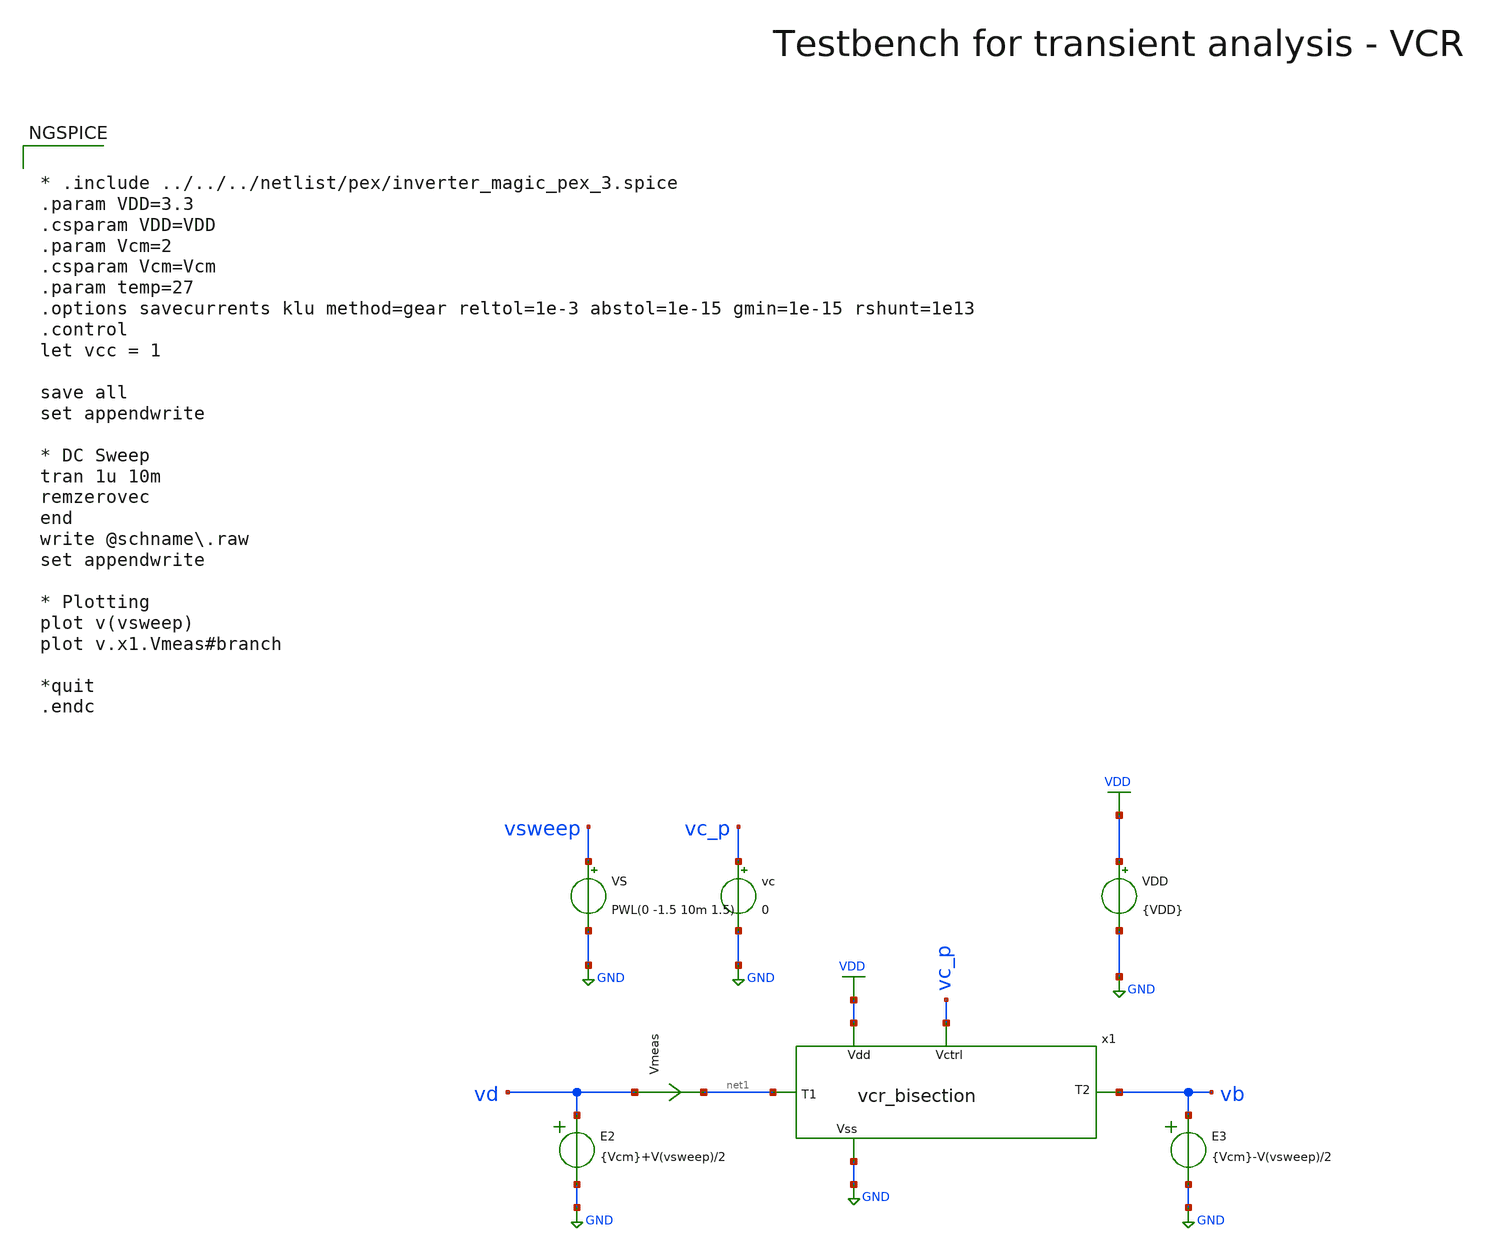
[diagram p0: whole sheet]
** sch_path: macros/voltage_controlled_resistors/macros/vcr_bisection/testbenches/xschem/res_tb_tran.sch
**.subckt res_tb_tran
VDD VDD GND {VDD}
VS vsweep GND PWL(0 -1.5 10m 1.5)
Vmeas vd net1 0
.save i(vmeas)
E2 vd GND VOL=' {Vcm}+V(vsweep)/2 '
E3 vb GND VOL=' {Vcm}-V(vsweep)/2 '
vc vc_p GND 0
x1 vc_p net1 vb VDD GND vcr_bisection
**** begin user architecture code

.lib cornerMOSlv.lib mos_tt
.lib cornerMOShv.lib mos_tt
.lib cornerRES.lib res_typ
.lib cornerDIO.lib dio_tt



* .include ../../../netlist/pex/inverter_magic_pex_3.spice
.param VDD=3.3
.csparam VDD=VDD
.param Vcm=2
.csparam Vcm=Vcm
.param temp=27
.options savecurrents klu method=gear reltol=1e-3 abstol=1e-15 gmin=1e-15 rshunt=1e13
.control
let vcc = 1

save all
set appendwrite

* DC Sweep
tran 1u 10m
remzerovec
end
write @schname\.raw
set appendwrite

* Plotting
plot v(vsweep)
plot v.x1.Vmeas#branch

*quit
.endc


**** end user architecture code
**.ends
.GLOBAL GND
.GLOBAL VDD
.end
